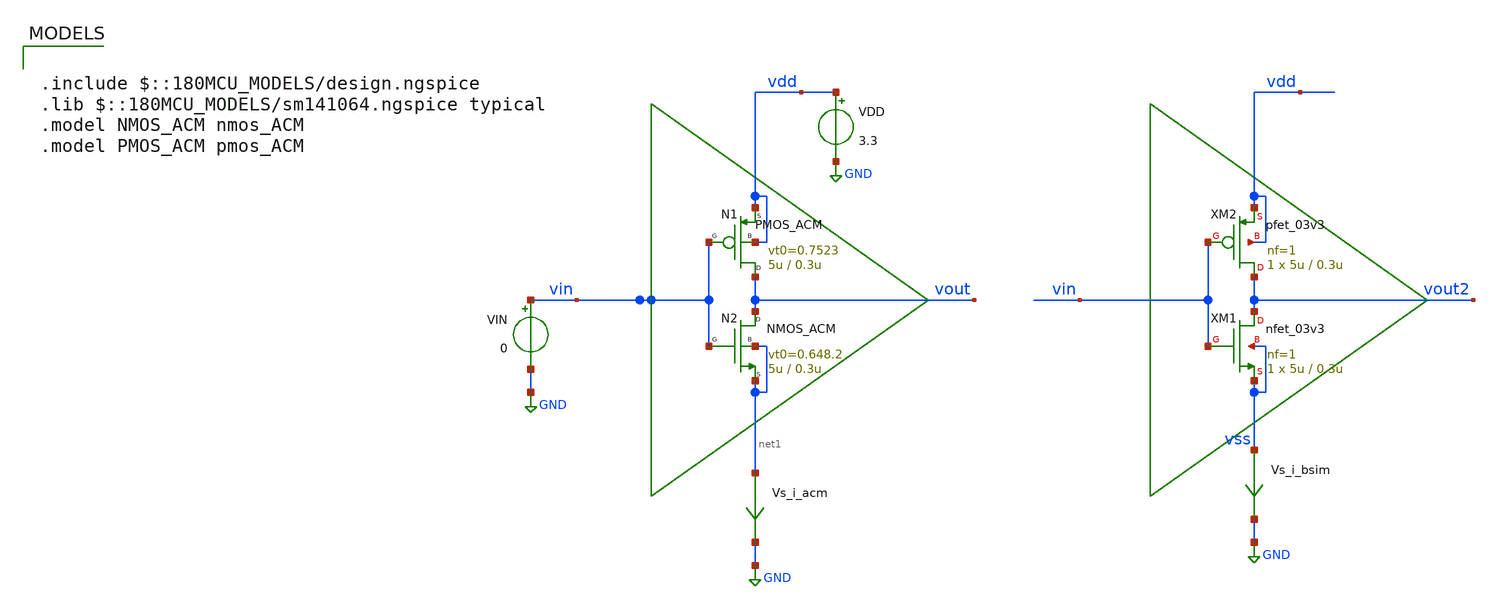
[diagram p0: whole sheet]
** sch_path: ihp_tutorials/ACM/TB_inv_acm_vt0.sch
**.subckt TB_inv_acm_vt0
VIN vin GND 0
VDD vdd GND 3.3
N2 vout vin net1 net1 NMOS_ACM w=5u l=0.3u n=1.37 is=1.06u vt0=0.648.2 sigma=26.3m zeta=6.7m
N1 vout vin vdd vdd PMOS_ACM w=5u l=0.3u n=1.42 is=0.35u vt0=0.7523 sigma=19.2m zeta=7m
Vs_i_bsim vss GND 0
.save i(vs_i_bsim)
XM1 vout2 vin vss vss nfet_03v3 L=0.3u W=5u nf=1 ad='int((nf+1)/2) * W/nf * 0.18u' as='int((nf+2)/2) * W/nf * 0.18u'
+ pd='2*int((nf+1)/2) * (W/nf + 0.18u)' ps='2*int((nf+2)/2) * (W/nf + 0.18u)' nrd='0.18u / W' nrs='0.18u / W'
+ sa=0 sb=0 sd=0 m=1
XM2 vout2 vin vdd vdd pfet_03v3 L=0.3u W=5u nf=1 ad='int((nf+1)/2) * W/nf * 0.18u' as='int((nf+2)/2) * W/nf * 0.18u'
+ pd='2*int((nf+1)/2) * (W/nf + 0.18u)' ps='2*int((nf+2)/2) * (W/nf + 0.18u)' nrd='0.18u / W' nrs='0.18u / W'
+ sa=0 sb=0 sd=0 m=1
Vs_i_acm net1 GND 0
.save i(vs_i_acm)
**** begin user architecture code

.include $::180MCU_MODELS/design.ngspice
.lib $::180MCU_MODELS/sm141064.ngspice typical
.model NMOS_ACM nmos_ACM
.model PMOS_ACM pmos_ACM



*.option gmin=1e-18
.control
pre_osdi /home/gmaranhao/Desktop/gf180_work/ACM/NMOS_ACM_2V0.osdi
pre_osdi /home/gmaranhao/Desktop/gf180_work/ACM/PMOS_ACM_2V0.osdi
save all

op
remzerovec
write TB_inv_acm_vt0.raw
set appendwrite

dc VIN 0 3.3 1m
remzerovec
write TB_inv_acm_vt0.raw
set appendwrite

.endc


**** end user architecture code
**.ends
.GLOBAL GND
.end
